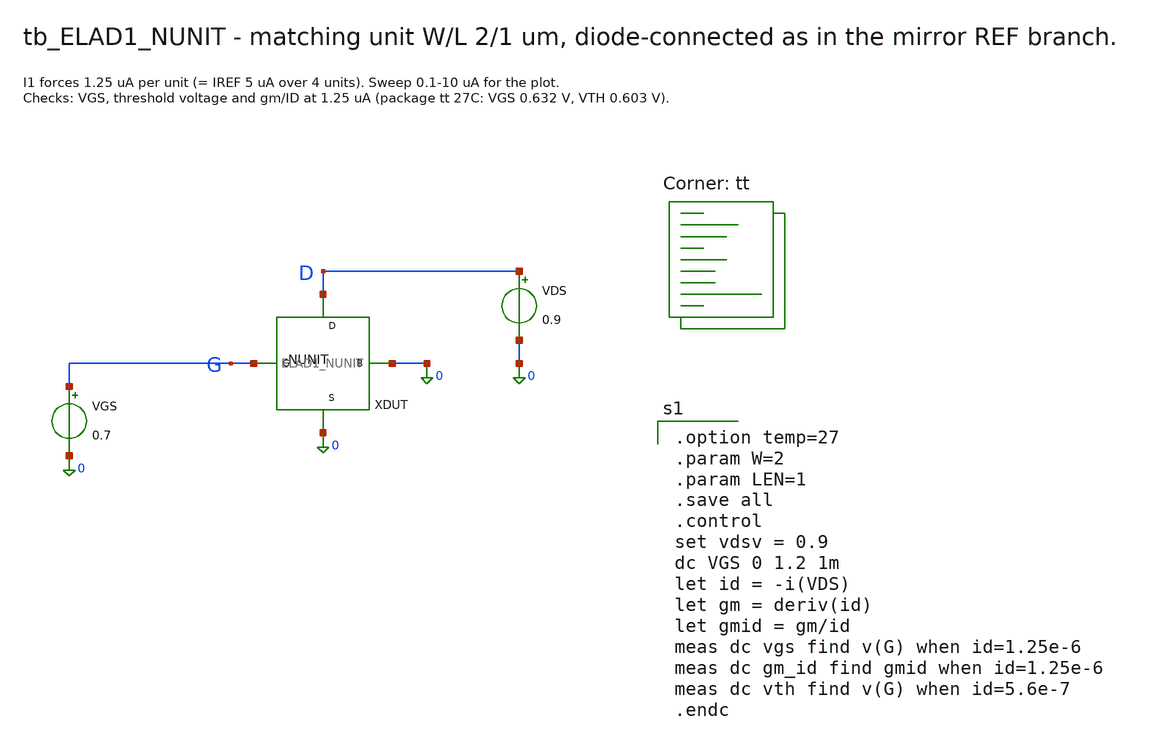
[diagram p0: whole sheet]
** sch_path: cells/ELAD1_NUNIT/schematic/tb_ELAD1_NUNIT.sch
**.subckt tb_ELAD1_NUNIT
XDUT D G 0 0 ELAD1_NUNIT
VGS G 0 0.7
VDS D 0 0.9
**** begin user architecture code

.option temp=27
.param W=2
.param LEN=1
.save all
.control
set vdsv = 0.9
dc VGS 0 1.2 1m
let id = -i(VDS)
let gm = deriv(id)
let gmid = gm/id
meas dc vgs find v(G) when id=1.25e-6
meas dc gm_id find gmid when id=1.25e-6
meas dc vth find v(G) when id=5.6e-7
.endc

.lib $::SKYWATER_MODELS/sky130.lib.spice tt
**** end user architecture code
**.ends

* expanding   symbol:  ELAD1_NUNIT.sym # of pins=4
** sym_path: cells/ELAD1_NUNIT/schematic/ELAD1_NUNIT.sym
** sch_path: cells/ELAD1_NUNIT/schematic/ELAD1_NUNIT.sch
.subckt ELAD1_NUNIT D G S B
*.iopin D
*.iopin G
*.iopin S
*.iopin B
XM D G S B sky130_fd_pr__nfet_01v8 L=1 W=2 nf=1 ad='int((1 + 1)/2) * 2 / 1 * 0.29' as='int((1 + 2)/2) * 2 / 1 * 0.29'
+ pd='2*int((1 + 1)/2) * (2 / 1 + 0.29)' ps='2*int((1 + 2)/2) * (2 / 1 + 0.29)' nrd='0.29 / 2 ' nrs='0.29 / 2 '
+ sa=0 sb=0 sd=0 mult=1 m=1
.ends

.end
